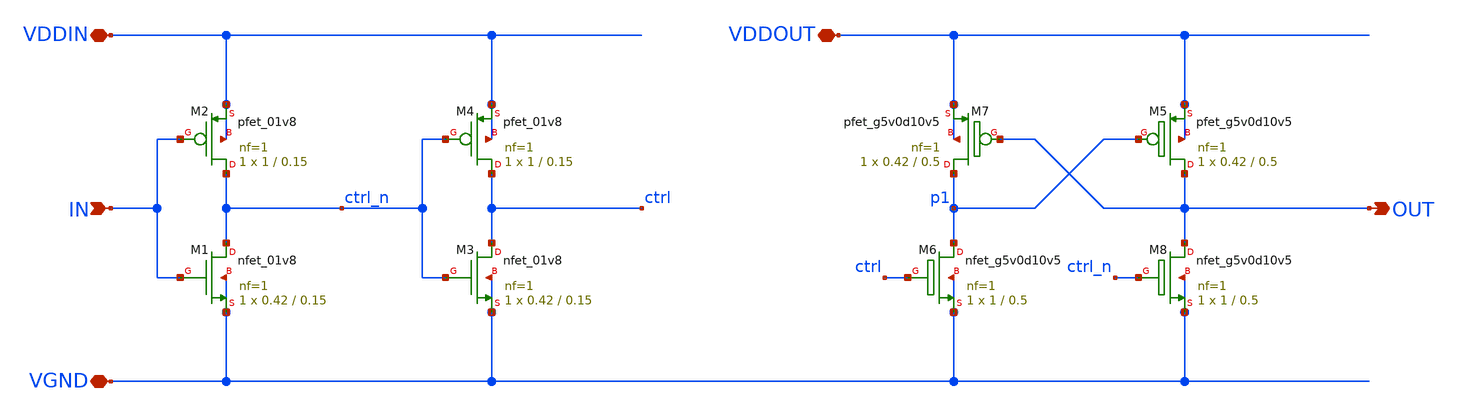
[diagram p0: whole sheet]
** sch_path: tt_um_tt08_aicd_playground/dependencies/sky130_leo_ip__levelshifter/xschem/sky130_leo_ip__levelshifter_up.sch
**.subckt sky130_leo_ip__levelshifter_up IN VGND VDDIN OUT VDDOUT
*.ipin IN
*.iopin VGND
*.iopin VDDIN
*.opin OUT
*.iopin VDDOUT
XM1 ctrl_n IN VGND VGND sky130_fd_pr__nfet_01v8 L=0.15 W=0.42 nf=1 ad='int((nf+1)/2) * W/nf * 0.29' as='int((nf+2)/2) * W/nf * 0.29'
+ pd='2*int((nf+1)/2) * (W/nf + 0.29)' ps='2*int((nf+2)/2) * (W/nf + 0.29)' nrd='0.29 / W' nrs='0.29 / W'
+ sa=0 sb=0 sd=0 mult=1 m=1
XM2 ctrl_n IN VDDIN VDDIN sky130_fd_pr__pfet_01v8 L=0.15 W=1 nf=1 ad='int((nf+1)/2) * W/nf * 0.29' as='int((nf+2)/2) * W/nf * 0.29'
+ pd='2*int((nf+1)/2) * (W/nf + 0.29)' ps='2*int((nf+2)/2) * (W/nf + 0.29)' nrd='0.29 / W' nrs='0.29 / W'
+ sa=0 sb=0 sd=0 mult=1 m=1
XM3 ctrl ctrl_n VGND VGND sky130_fd_pr__nfet_01v8 L=0.15 W=0.42 nf=1 ad='int((nf+1)/2) * W/nf * 0.29'
+ as='int((nf+2)/2) * W/nf * 0.29' pd='2*int((nf+1)/2) * (W/nf + 0.29)' ps='2*int((nf+2)/2) * (W/nf + 0.29)'
+ nrd='0.29 / W' nrs='0.29 / W' sa=0 sb=0 sd=0 mult=1 m=1
XM4 ctrl ctrl_n VDDIN VDDIN sky130_fd_pr__pfet_01v8 L=0.15 W=1 nf=1 ad='int((nf+1)/2) * W/nf * 0.29'
+ as='int((nf+2)/2) * W/nf * 0.29' pd='2*int((nf+1)/2) * (W/nf + 0.29)' ps='2*int((nf+2)/2) * (W/nf + 0.29)'
+ nrd='0.29 / W' nrs='0.29 / W' sa=0 sb=0 sd=0 mult=1 m=1
XM5 OUT p1 VDDOUT VDDOUT sky130_fd_pr__pfet_g5v0d10v5 L=0.5 W=0.42 nf=1 ad='int((nf+1)/2) * W/nf * 0.29'
+ as='int((nf+2)/2) * W/nf * 0.29' pd='2*int((nf+1)/2) * (W/nf + 0.29)' ps='2*int((nf+2)/2) * (W/nf + 0.29)'
+ nrd='0.29 / W' nrs='0.29 / W' sa=0 sb=0 sd=0 mult=1 m=1
XM6 p1 ctrl VGND VGND sky130_fd_pr__nfet_g5v0d10v5 L=0.5 W=1 nf=1 ad='int((nf+1)/2) * W/nf * 0.29' as='int((nf+2)/2) * W/nf * 0.29'
+ pd='2*int((nf+1)/2) * (W/nf + 0.29)' ps='2*int((nf+2)/2) * (W/nf + 0.29)' nrd='0.29 / W' nrs='0.29 / W'
+ sa=0 sb=0 sd=0 mult=1 m=1
XM7 p1 OUT VDDOUT VDDOUT sky130_fd_pr__pfet_g5v0d10v5 L=0.5 W=0.42 nf=1 ad='int((nf+1)/2) * W/nf * 0.29'
+ as='int((nf+2)/2) * W/nf * 0.29' pd='2*int((nf+1)/2) * (W/nf + 0.29)' ps='2*int((nf+2)/2) * (W/nf + 0.29)'
+ nrd='0.29 / W' nrs='0.29 / W' sa=0 sb=0 sd=0 mult=1 m=1
XM8 OUT ctrl_n VGND VGND sky130_fd_pr__nfet_g5v0d10v5 L=0.5 W=1 nf=1 ad='int((nf+1)/2) * W/nf * 0.29'
+ as='int((nf+2)/2) * W/nf * 0.29' pd='2*int((nf+1)/2) * (W/nf + 0.29)' ps='2*int((nf+2)/2) * (W/nf + 0.29)'
+ nrd='0.29 / W' nrs='0.29 / W' sa=0 sb=0 sd=0 mult=1 m=1
**.ends
.end
